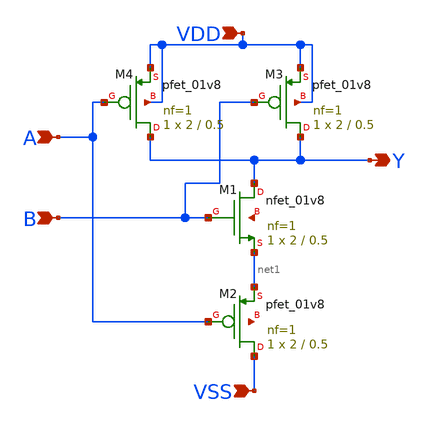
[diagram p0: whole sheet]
** sch_path: Layouts and Schematics/Spice Sim and Schem/untitled-2.sch
**.subckt untitled-2 A B VSS Y VDD
*.ipin A
*.ipin B
*.ipin VSS
*.opin Y
*.ipin VDD
XM1 Y B net1 net2 sky130_fd_pr__nfet_01v8 L=0.5 W=2 nf=1 ad='int((nf+1)/2) * W/nf * 0.29' as='int((nf+2)/2) * W/nf * 0.29'
+ pd='2*int((nf+1)/2) * (W/nf + 0.29)' ps='2*int((nf+2)/2) * (W/nf + 0.29)' nrd='0.29 / W' nrs='0.29 / W'
+ sa=0 sb=0 sd=0 mult=1 m=1
XM3 Y B VDD VDD sky130_fd_pr__pfet_01v8 L=0.5 W=2 nf=1 ad='int((nf+1)/2) * W/nf * 0.29' as='int((nf+2)/2) * W/nf * 0.29'
+ pd='2*int((nf+1)/2) * (W/nf + 0.29)' ps='2*int((nf+2)/2) * (W/nf + 0.29)' nrd='0.29 / W' nrs='0.29 / W'
+ sa=0 sb=0 sd=0 mult=1 m=1
XM4 Y A VDD VDD sky130_fd_pr__pfet_01v8 L=0.5 W=2 nf=1 ad='int((nf+1)/2) * W/nf * 0.29' as='int((nf+2)/2) * W/nf * 0.29'
+ pd='2*int((nf+1)/2) * (W/nf + 0.29)' ps='2*int((nf+2)/2) * (W/nf + 0.29)' nrd='0.29 / W' nrs='0.29 / W'
+ sa=0 sb=0 sd=0 mult=1 m=1
XM2 VSS A net1 net3 sky130_fd_pr__pfet_01v8 L=0.5 W=2 nf=1 ad='int((nf+1)/2) * W/nf * 0.29' as='int((nf+2)/2) * W/nf * 0.29'
+ pd='2*int((nf+1)/2) * (W/nf + 0.29)' ps='2*int((nf+2)/2) * (W/nf + 0.29)' nrd='0.29 / W' nrs='0.29 / W'
+ sa=0 sb=0 sd=0 mult=1 m=1
**.ends
.end
